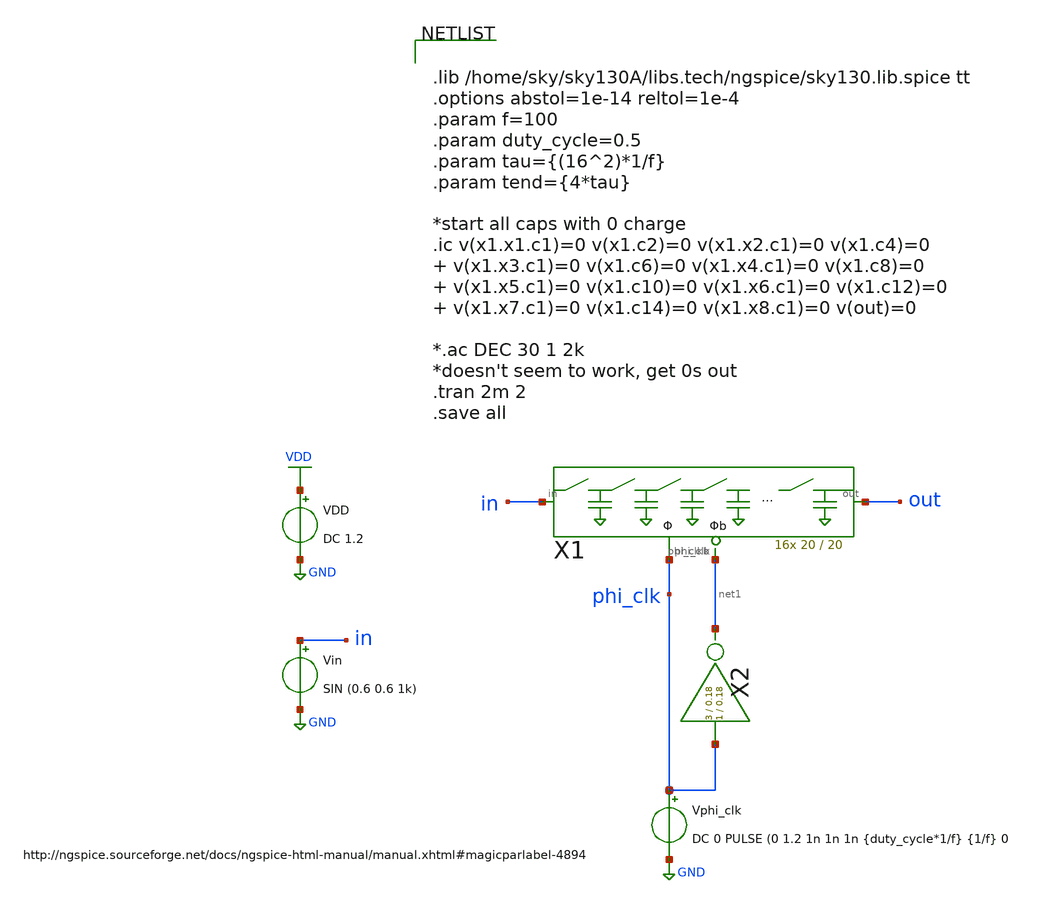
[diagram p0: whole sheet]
** sch_path: xschem/untitled-6.sch
**.subckt untitled-6
Vin in GND SIN (0.6 0.6 1k)
VDD VDD GND DC 1.2
Vphi_clk phi_clk GND DC 0 PULSE (0 1.2 1n 1n 1n {duty_cycle*1/f} {1/f} 0
X1 in out phi_clk net1 16switchcaps W=20 L=20
X2 phi_clk net1 inv Wpmos=3 Lpmos=0.18 Wnmos=1 Lnmos=0.18
**** begin user architecture code


.lib /home/sky/sky130A/libs.tech/ngspice/sky130.lib.spice tt
.options abstol=1e-14 reltol=1e-4
.param f=100
.param duty_cycle=0.5
.param tau={(16^2)*1/f}
.param tend={4*tau}

*start all caps with 0 charge
.ic v(x1.x1.c1)=0 v(x1.c2)=0 v(x1.x2.c1)=0 v(x1.c4)=0   v(x1.x3.c1)=0 v(x1.c6)=0 v(x1.x4.c1)=0
+ v(x1.c8)=0   v(x1.x5.c1)=0 v(x1.c10)=0 v(x1.x6.c1)=0 v(x1.c12)=0   v(x1.x7.c1)=0 v(x1.c14)=0 v(x1.x8.c1)=0
+ v(out)=0

*.ac DEC 30 1 2k
*doesn't seem to work, get 0s out
.tran 2m 2
.save all


**** end user architecture code
**.ends
.GLOBAL GND
.GLOBAL VDD
.end
